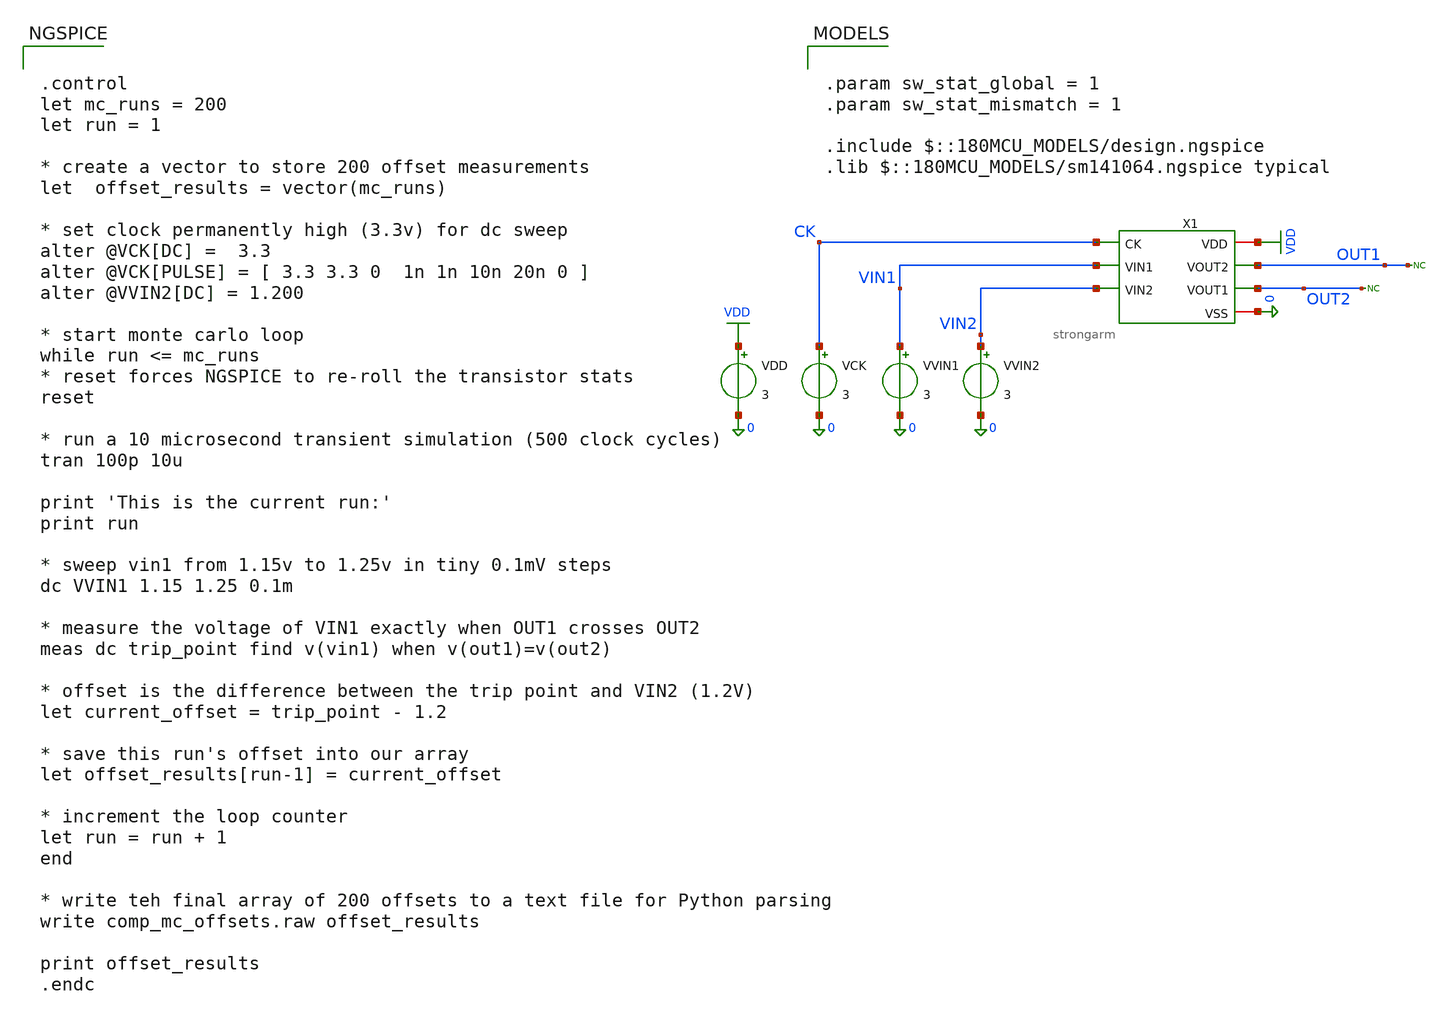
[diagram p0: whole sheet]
** sch_path: comparator/schematic/mc_backup_files/strongarm_mc_tb_backup.sch
**.subckt strongarm_mc_tb_backup
X1 VDD CK OUT1 OUT2 VIN1 VIN2 0 strongarm
VVIN2 VIN2 0 3
VVIN1 VIN1 0 3
VDD VDD 0 3
VCK CK 0 3
* noconn OUT2
* noconn OUT1
**** begin user architecture code

.param sw_stat_global = 1
.param sw_stat_mismatch = 1

.include $::180MCU_MODELS/design.ngspice
.lib $::180MCU_MODELS/sm141064.ngspice typical



.control
let mc_runs = 200
let run = 1

* create a vector to store 200 offset measurements
let  offset_results = vector(mc_runs)

* set clock permanently high (3.3v) for dc sweep
alter @VCK[DC] =  3.3
alter @VCK[PULSE] = [ 3.3 3.3 0  1n 1n 10n 20n 0 ]
alter @VVIN2[DC] = 1.200

* start monte carlo loop
while run <= mc_runs
* reset forces NGSPICE to re-roll the transistor stats
reset

* run a 10 microsecond transient simulation (500 clock cycles)
tran 100p 10u

print 'This is the current run:'
print run

* sweep vin1 from 1.15v to 1.25v in tiny 0.1mV steps
dc VVIN1 1.15 1.25 0.1m

* measure the voltage of VIN1 exactly when OUT1 crosses OUT2
meas dc trip_point find v(vin1) when v(out1)=v(out2)

* offset is the difference between the trip point and VIN2 (1.2V)
let current_offset = trip_point - 1.2

* save this run's offset into our array
let offset_results[run-1] = current_offset

* increment the loop counter
let run = run + 1
end

* write teh final array of 200 offsets to a text file for Python parsing
write comp_mc_offsets.raw offset_results

print offset_results
.endc

**** end user architecture code
**.ends

* expanding   symbol:  comparator/schematic/strongarm.sym # of pins=7
** sym_path: comparator/schematic/strongarm.sym
** sch_path: comparator/schematic/strongarm.sch
.subckt strongarm VDD CK VOUT2 VOUT1 VIN1 VIN2 VSS
*.opin VOUT1
*.opin VOUT2
*.ipin VIN1
*.ipin VIN2
*.ipin CK
*.iopin VDD
*.iopin VSS
XM1 VOUT2 VOUT1 net1 net1 nfet_03v3 L=0.28u W=0.22u nf=1 ad='int((nf+1)/2) * W/nf * 0.18u' as='int((nf+2)/2)
+ * W/nf * 0.18u' pd='2*int((nf+1)/2) * (W/nf + 0.18u)' ps='2*int((nf+2)/2) * (W/nf + 0.18u)' nrd='0.18u
+ / W' nrs='0.18u / W' sa=0 sb=0 sd=0 m=1
XM2 VOUT1 VOUT2 VDD VDD pfet_03v3 L=0.28u W=0.22u nf=1 ad='int((nf+1)/2) * W/nf * 0.18u' as='int((nf+2)/2)
+ * W/nf * 0.18u' pd='2*int((nf+1)/2) * (W/nf + 0.18u)' ps='2*int((nf+2)/2) * (W/nf + 0.18u)' nrd='0.18u
+ / W' nrs='0.18u / W' sa=0 sb=0 sd=0 m=1
XM3 VOUT1 CK VDD VDD pfet_03v3 L=0.28u W=0.22u nf=1 ad='int((nf+1)/2) * W/nf * 0.18u' as='int((nf+2)/2)
+ * W/nf * 0.18u' pd='2*int((nf+1)/2) * (W/nf + 0.18u)' ps='2*int((nf+2)/2) * (W/nf + 0.18u)' nrd='0.18u
+ / W' nrs='0.18u / W' sa=0 sb=0 sd=0 m=1
XM4 net3 CK VDD VDD pfet_03v3 L=0.28u W=0.22u nf=1 ad='int((nf+1)/2) * W/nf * 0.18u' as='int((nf+2)/2)
+ * W/nf * 0.18u' pd='2*int((nf+1)/2) * (W/nf + 0.18u)' ps='2*int((nf+2)/2) * (W/nf + 0.18u)' nrd='0.18u
+ / W' nrs='0.18u / W' sa=0 sb=0 sd=0 m=1
XM5 net1 CK VDD VDD pfet_03v3 L=0.28u W=0.22u nf=1 ad='int((nf+1)/2) * W/nf * 0.18u' as='int((nf+2)/2)
+ * W/nf * 0.18u' pd='2*int((nf+1)/2) * (W/nf + 0.18u)' ps='2*int((nf+2)/2) * (W/nf + 0.18u)' nrd='0.18u
+ / W' nrs='0.18u / W' sa=0 sb=0 sd=0 m=1
XM6 VOUT2 CK VDD VDD pfet_03v3 L=0.28u W=0.22u nf=1 ad='int((nf+1)/2) * W/nf * 0.18u' as='int((nf+2)/2)
+ * W/nf * 0.18u' pd='2*int((nf+1)/2) * (W/nf + 0.18u)' ps='2*int((nf+2)/2) * (W/nf + 0.18u)' nrd='0.18u
+ / W' nrs='0.18u / W' sa=0 sb=0 sd=0 m=1
XM7 VOUT2 VOUT1 VDD VDD pfet_03v3 L=0.28u W=0.22u nf=1 ad='int((nf+1)/2) * W/nf * 0.18u' as='int((nf+2)/2)
+ * W/nf * 0.18u' pd='2*int((nf+1)/2) * (W/nf + 0.18u)' ps='2*int((nf+2)/2) * (W/nf + 0.18u)' nrd='0.18u
+ / W' nrs='0.18u / W' sa=0 sb=0 sd=0 m=1
XM8 net1 VIN2 net2 net2 nfet_03v3 L=0.28u W=0.22u nf=1 ad='int((nf+1)/2) * W/nf * 0.18u' as='int((nf+2)/2)
+ * W/nf * 0.18u' pd='2*int((nf+1)/2) * (W/nf + 0.18u)' ps='2*int((nf+2)/2) * (W/nf + 0.18u)' nrd='0.18u
+ / W' nrs='0.18u / W' sa=0 sb=0 sd=0 m=1
XM9 VOUT1 VOUT2 net3 net3 nfet_03v3 L=0.28u W=0.22u nf=1 ad='int((nf+1)/2) * W/nf * 0.18u' as='int((nf+2)/2)
+ * W/nf * 0.18u' pd='2*int((nf+1)/2) * (W/nf + 0.18u)' ps='2*int((nf+2)/2) * (W/nf + 0.18u)' nrd='0.18u
+ / W' nrs='0.18u / W' sa=0 sb=0 sd=0 m=1
XM10 net3 VIN1 net2 net2 nfet_03v3 L=0.28u W=0.22u nf=1 ad='int((nf+1)/2) * W/nf * 0.18u' as='int((nf+2)/2)
+ * W/nf * 0.18u' pd='2*int((nf+1)/2) * (W/nf + 0.18u)' ps='2*int((nf+2)/2) * (W/nf + 0.18u)' nrd='0.18u
+ / W' nrs='0.18u / W' sa=0 sb=0 sd=0 m=1
XM11 net2 CK VSS net2 nfet_03v3 L=0.28u W=0.22u nf=1 ad='int((nf+1)/2) * W/nf * 0.18u' as='int((nf+2)/2)
+ * W/nf * 0.18u' pd='2*int((nf+1)/2) * (W/nf + 0.18u)' ps='2*int((nf+2)/2) * (W/nf + 0.18u)' nrd='0.18u
+ / W' nrs='0.18u / W' sa=0 sb=0 sd=0 m=1
.ends

.GLOBAL VDD
.end
